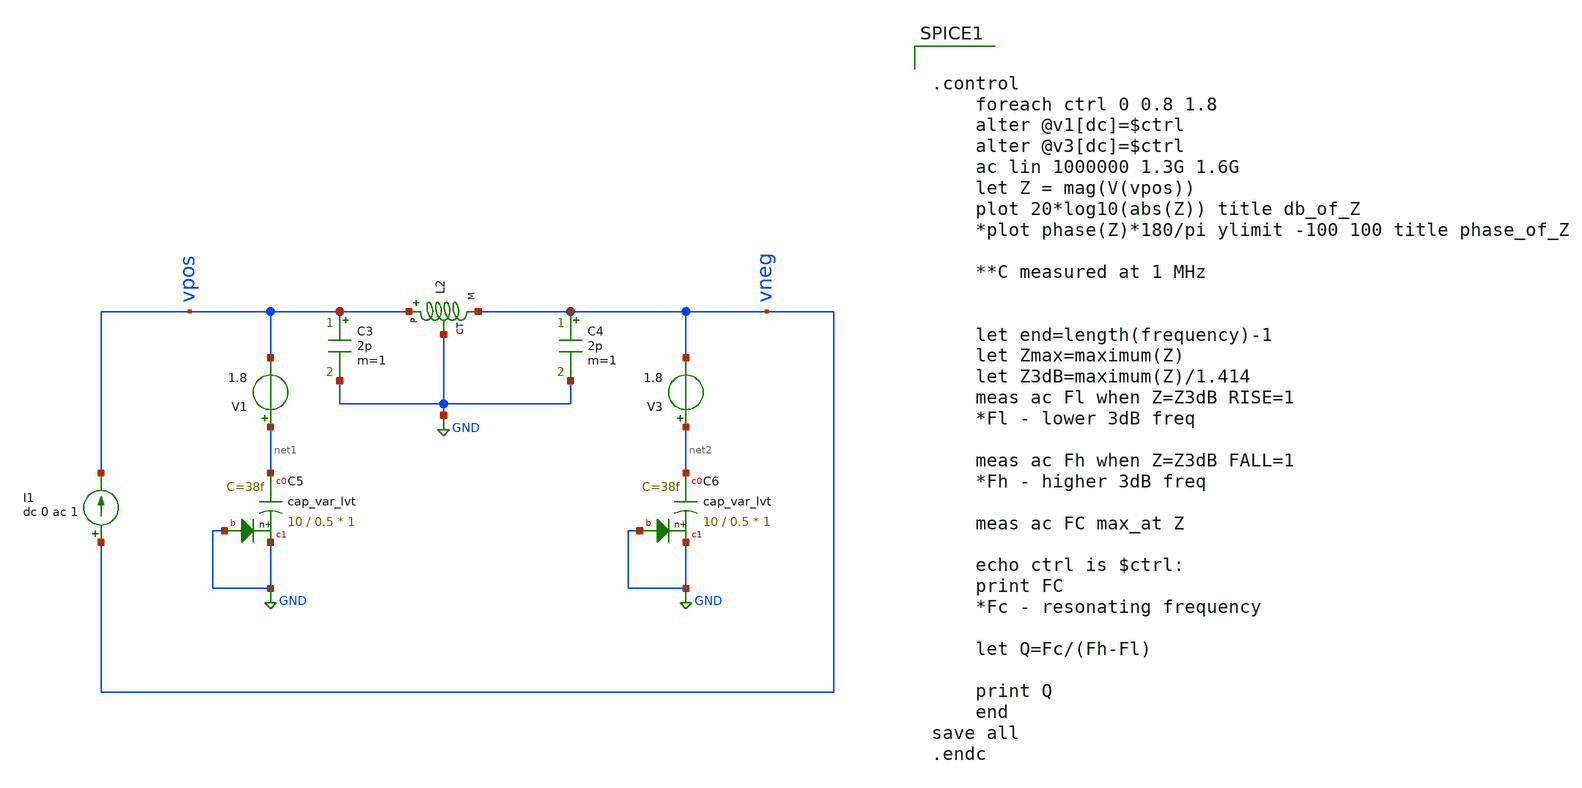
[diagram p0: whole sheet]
** sch_path: tank_meas/tank_Q_meas.sch
**.subckt tank_Q_meas
XL2 vpos vneg GND GND sky130_fd_pr__ind_05_220
C3 vpos GND 2p m=1
C4 vneg GND 2p m=1
XC5 net1 GND GND sky130_fd_pr__cap_var_lvt W=10 L=0.5 VM=1 m=1
V1 net1 vpos 1.8
XC6 net2 GND GND sky130_fd_pr__cap_var_lvt W=10 L=0.5 VM=1 m=1
V3 net2 vneg 1.8
I1 vneg vpos dc 0 ac 1
**** begin user architecture code


.option wnflag = 1
.lib /usr/local/share/pdk/sky130A/libs.tech/ngspice/sky130.lib.spice tt
.include /usr/local/share/pdk/sky130A/libs.ref/sky130_fd_pr/spice/sky130_fd_pr__ind_05_220.model.spice
.param mc_mm_switch=0




.control
	foreach ctrl 0 0.8 1.8
	alter @v1[dc]=$ctrl
	alter @v3[dc]=$ctrl
	ac lin 1000000 1.3G 1.6G
	let Z = mag(V(vpos))
	plot 20*log10(abs(Z)) title db_of_Z
	*plot phase(Z)*180/pi ylimit -100 100 title phase_of_Z

	**C measured at 1 MHz


	let end=length(frequency)-1
	let Zmax=maximum(Z)
	let Z3dB=maximum(Z)/1.414
	meas ac Fl when Z=Z3dB RISE=1
	*Fl - lower 3dB freq

	meas ac Fh when Z=Z3dB FALL=1
	*Fh - higher 3dB freq

	meas ac FC max_at Z

	echo ctrl is $ctrl:
	print FC
	*Fc - resonating frequency

	let Q=Fc/(Fh-Fl)

	print Q
	end
save all
.endc


**** end user architecture code
**.ends
.GLOBAL GND
.end
